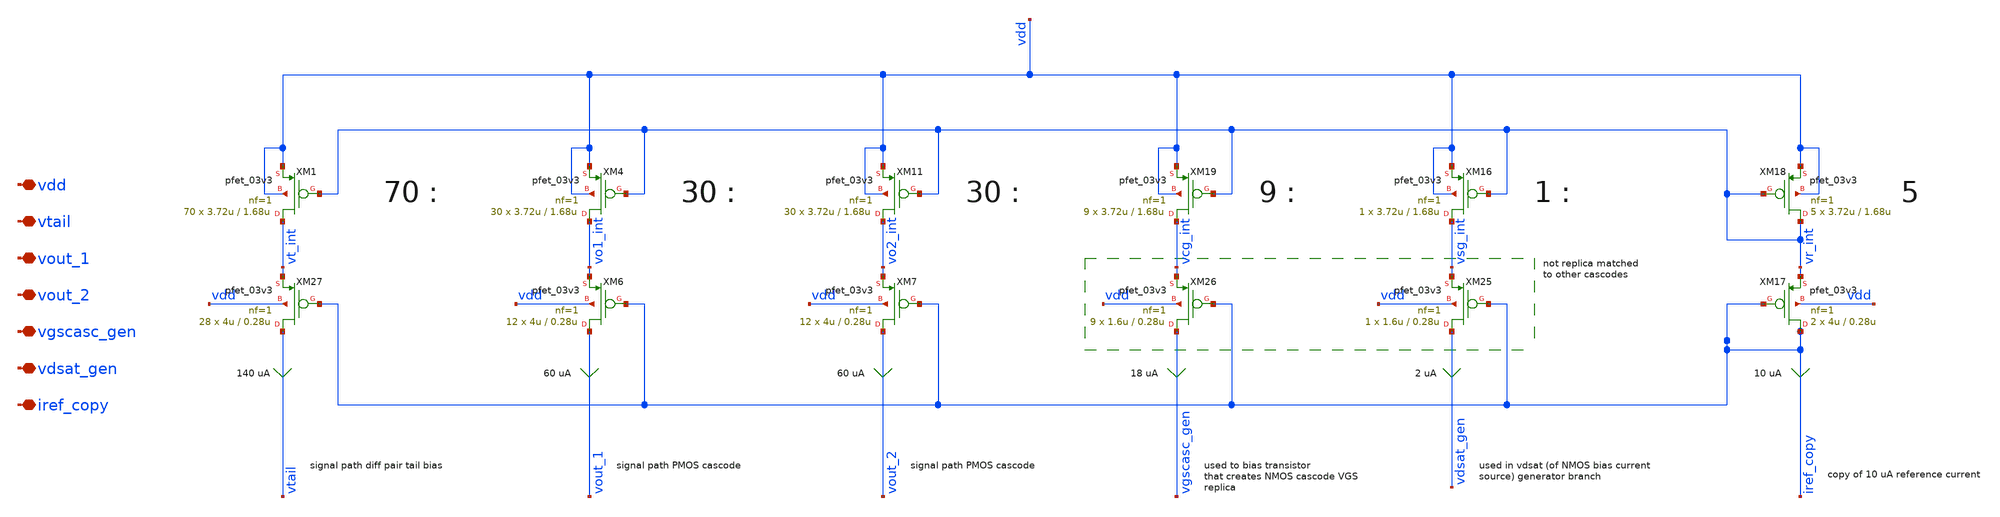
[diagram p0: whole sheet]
** sch_path: xschem/archive/ota/s1_pmos_bias.sch
**.subckt s1_pmos_bias vdd vtail vout_1 vout_2 vgscasc_gen vdsat_gen iref_copy
*.iopin vdd
*.iopin vtail
*.iopin vout_1
*.iopin vout_2
*.iopin vgscasc_gen
*.iopin vdsat_gen
*.iopin iref_copy
XM1 vt_int vr_int vdd vdd pfet_03v3 L=1.68u W=3.72u nf=1 ad='int((nf+1)/2) * W/nf * 0.18u' as='int((nf+2)/2) * W/nf * 0.18u'
+ pd='2*int((nf+1)/2) * (W/nf + 0.18u)' ps='2*int((nf+2)/2) * (W/nf + 0.18u)' nrd='0.18u / W' nrs='0.18u / W'
+ sa=0 sb=0 sd=0 m=70
XM7 vout_2 iref_copy vo2_int vdd pfet_03v3 L=0.28u W=4u nf=1 ad='int((nf+1)/2) * W/nf * 0.18u' as='int((nf+2)/2) * W/nf * 0.18u'
+ pd='2*int((nf+1)/2) * (W/nf + 0.18u)' ps='2*int((nf+2)/2) * (W/nf + 0.18u)' nrd='0.18u / W' nrs='0.18u / W'
+ sa=0 sb=0 sd=0 m=12
XM17 iref_copy iref_copy vr_int vdd pfet_03v3 L=0.28u W=4u nf=1 ad='int((nf+1)/2) * W/nf * 0.18u' as='int((nf+2)/2) * W/nf * 0.18u'
+ pd='2*int((nf+1)/2) * (W/nf + 0.18u)' ps='2*int((nf+2)/2) * (W/nf + 0.18u)' nrd='0.18u / W' nrs='0.18u / W'
+ sa=0 sb=0 sd=0 m=2
XM18 vr_int vr_int vdd vdd pfet_03v3 L=1.68u W=3.72u nf=1 ad='int((nf+1)/2) * W/nf * 0.18u' as='int((nf+2)/2) * W/nf * 0.18u'
+ pd='2*int((nf+1)/2) * (W/nf + 0.18u)' ps='2*int((nf+2)/2) * (W/nf + 0.18u)' nrd='0.18u / W' nrs='0.18u / W'
+ sa=0 sb=0 sd=0 m=5
XM4 vo1_int vr_int vdd vdd pfet_03v3 L=1.68u W=3.72u nf=1 ad='int((nf+1)/2) * W/nf * 0.18u' as='int((nf+2)/2) * W/nf * 0.18u'
+ pd='2*int((nf+1)/2) * (W/nf + 0.18u)' ps='2*int((nf+2)/2) * (W/nf + 0.18u)' nrd='0.18u / W' nrs='0.18u / W'
+ sa=0 sb=0 sd=0 m=30
XM16 vsg_int vr_int vdd vdd pfet_03v3 L=1.68u W=3.72u nf=1 ad='int((nf+1)/2) * W/nf * 0.18u' as='int((nf+2)/2) * W/nf * 0.18u'
+ pd='2*int((nf+1)/2) * (W/nf + 0.18u)' ps='2*int((nf+2)/2) * (W/nf + 0.18u)' nrd='0.18u / W' nrs='0.18u / W'
+ sa=0 sb=0 sd=0 m=1
XM19 vcg_int vr_int vdd vdd pfet_03v3 L=1.68u W=3.72u nf=1 ad='int((nf+1)/2) * W/nf * 0.18u' as='int((nf+2)/2) * W/nf * 0.18u'
+ pd='2*int((nf+1)/2) * (W/nf + 0.18u)' ps='2*int((nf+2)/2) * (W/nf + 0.18u)' nrd='0.18u / W' nrs='0.18u / W'
+ sa=0 sb=0 sd=0 m=9
XM11 vo2_int vr_int vdd vdd pfet_03v3 L=1.68u W=3.72u nf=1 ad='int((nf+1)/2) * W/nf * 0.18u' as='int((nf+2)/2) * W/nf * 0.18u'
+ pd='2*int((nf+1)/2) * (W/nf + 0.18u)' ps='2*int((nf+2)/2) * (W/nf + 0.18u)' nrd='0.18u / W' nrs='0.18u / W'
+ sa=0 sb=0 sd=0 m=30
XM6 vout_1 iref_copy vo1_int vdd pfet_03v3 L=0.28u W=4u nf=1 ad='int((nf+1)/2) * W/nf * 0.18u' as='int((nf+2)/2) * W/nf * 0.18u'
+ pd='2*int((nf+1)/2) * (W/nf + 0.18u)' ps='2*int((nf+2)/2) * (W/nf + 0.18u)' nrd='0.18u / W' nrs='0.18u / W'
+ sa=0 sb=0 sd=0 m=12
XM25 vdsat_gen iref_copy vsg_int vdd pfet_03v3 L=0.28u W=1.6u nf=1 ad='int((nf+1)/2) * W/nf * 0.18u'
+ as='int((nf+2)/2) * W/nf * 0.18u' pd='2*int((nf+1)/2) * (W/nf + 0.18u)' ps='2*int((nf+2)/2) * (W/nf + 0.18u)'
+ nrd='0.18u / W' nrs='0.18u / W' sa=0 sb=0 sd=0 m=1
XM26 vgscasc_gen iref_copy vcg_int vdd pfet_03v3 L=0.28u W=1.6u nf=1 ad='int((nf+1)/2) * W/nf * 0.18u'
+ as='int((nf+2)/2) * W/nf * 0.18u' pd='2*int((nf+1)/2) * (W/nf + 0.18u)' ps='2*int((nf+2)/2) * (W/nf + 0.18u)'
+ nrd='0.18u / W' nrs='0.18u / W' sa=0 sb=0 sd=0 m=9
XM27 vtail iref_copy vt_int vdd pfet_03v3 L=0.28u W=4u nf=1 ad='int((nf+1)/2) * W/nf * 0.18u' as='int((nf+2)/2) * W/nf * 0.18u'
+ pd='2*int((nf+1)/2) * (W/nf + 0.18u)' ps='2*int((nf+2)/2) * (W/nf + 0.18u)' nrd='0.18u / W' nrs='0.18u / W'
+ sa=0 sb=0 sd=0 m=28
**.ends
.end
